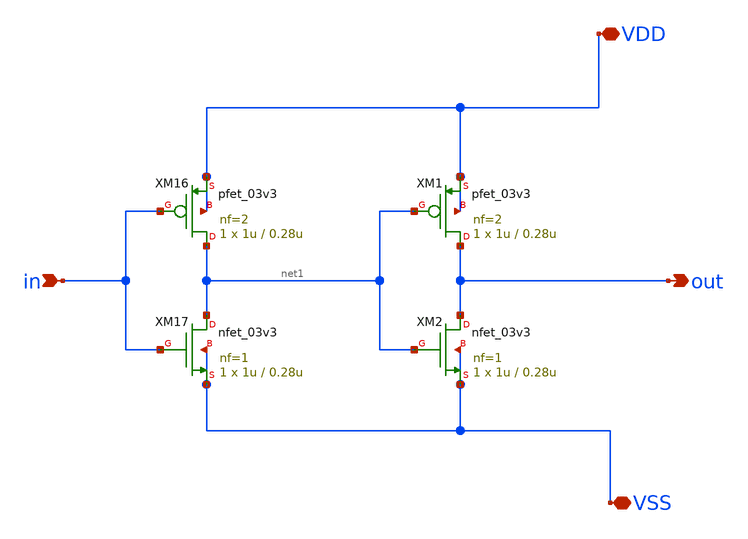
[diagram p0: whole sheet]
** sch_path: designs/libs/core_vco/vco_buffer/vco_buffer_updated.sch
**.subckt vco_buffer_updated in out VDD VSS
*.ipin in
*.opin out
*.iopin VDD
*.iopin VSS
XM16 net1 in VDD VDD pfet_03v3 L=0.28u W=1u nf=2 ad='int((nf+1)/2) * W/nf * 0.18u' as='int((nf+2)/2) * W/nf * 0.18u'
+ pd='2*int((nf+1)/2) * (W/nf + 0.18u)' ps='2*int((nf+2)/2) * (W/nf + 0.18u)' nrd='0.18u / W' nrs='0.18u / W'
+ sa=0 sb=0 sd=0 m=1
XM17 net1 in VSS VSS nfet_03v3 L=0.28u W=1u nf=1 ad='int((nf+1)/2) * W/nf * 0.18u' as='int((nf+2)/2) * W/nf * 0.18u'
+ pd='2*int((nf+1)/2) * (W/nf + 0.18u)' ps='2*int((nf+2)/2) * (W/nf + 0.18u)' nrd='0.18u / W' nrs='0.18u / W'
+ sa=0 sb=0 sd=0 m=1
XM2 out net1 VSS VSS nfet_03v3 L=0.28u W=1u nf=1 ad='int((nf+1)/2) * W/nf * 0.18u' as='int((nf+2)/2) * W/nf * 0.18u'
+ pd='2*int((nf+1)/2) * (W/nf + 0.18u)' ps='2*int((nf+2)/2) * (W/nf + 0.18u)' nrd='0.18u / W' nrs='0.18u / W'
+ sa=0 sb=0 sd=0 m=1
XM1 out net1 VDD VDD pfet_03v3 L=0.28u W=1u nf=2 ad='int((nf+1)/2) * W/nf * 0.18u' as='int((nf+2)/2) * W/nf * 0.18u'
+ pd='2*int((nf+1)/2) * (W/nf + 0.18u)' ps='2*int((nf+2)/2) * (W/nf + 0.18u)' nrd='0.18u / W' nrs='0.18u / W'
+ sa=0 sb=0 sd=0 m=1
**.ends
.end
